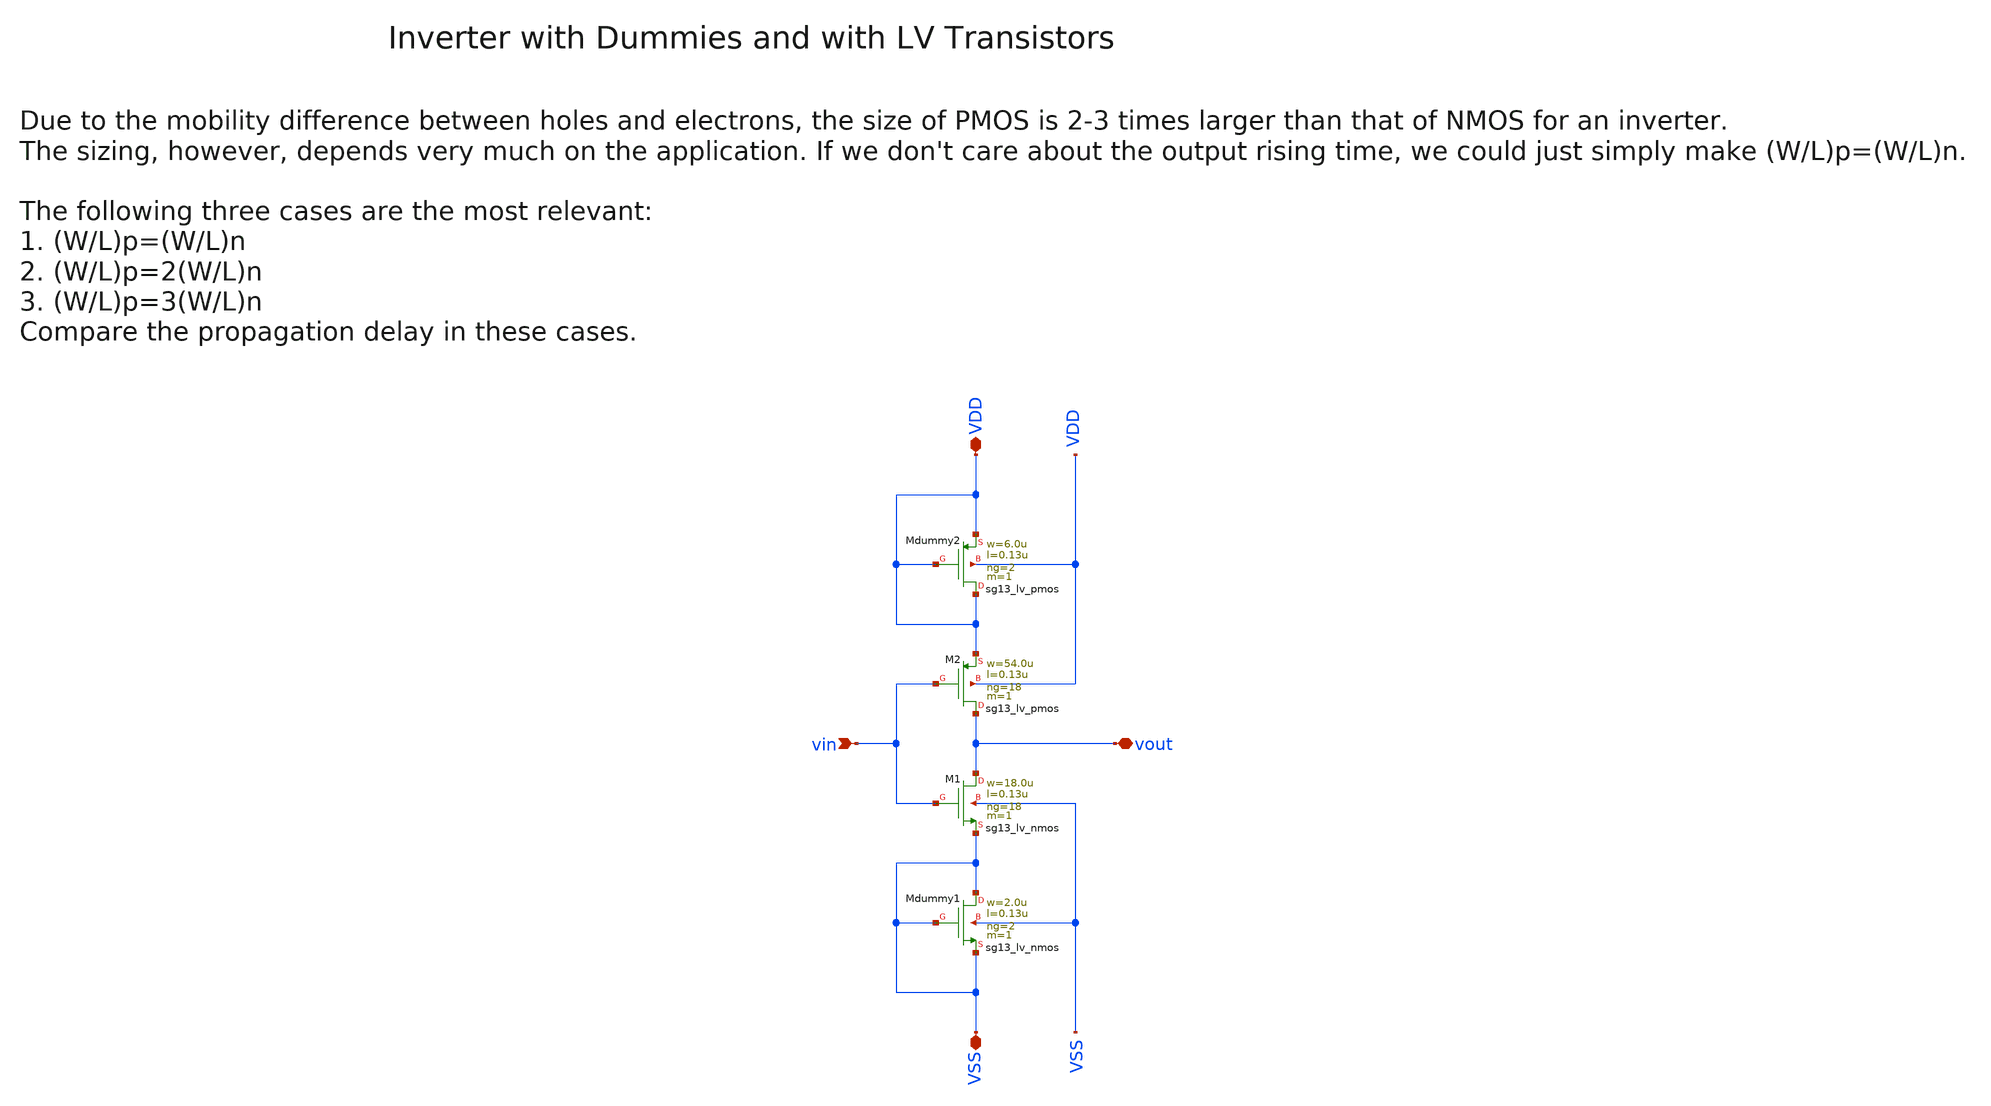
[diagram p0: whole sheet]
** sch_path: ihp130/macros/iqmod/schematic/xschem/iqmod_mixer_se2diff_inv_NF18.sch
**.subckt iqmod_mixer_se2diff_inv_NF18 vin VDD VSS vout
*.ipin vin
*.iopin VDD
*.iopin VSS
*.iopin vout
XM1 vout vin VSS VSS sg13_lv_nmos w=18.0u l=0.13u ng=18 m=1 mm_ok=1
XM2 vout vin VDD VDD sg13_lv_pmos w=54.0u l=0.13u ng=18 m=1 mm_ok=1
XMdummy1 VSS VSS VSS VSS sg13_lv_nmos w=2.0u l=0.13u ng=2 m=1 mm_ok=1
XMdummy2 VDD VDD VDD VDD sg13_lv_pmos w=6.0u l=0.13u ng=2 m=1 mm_ok=1
**.ends
.end
